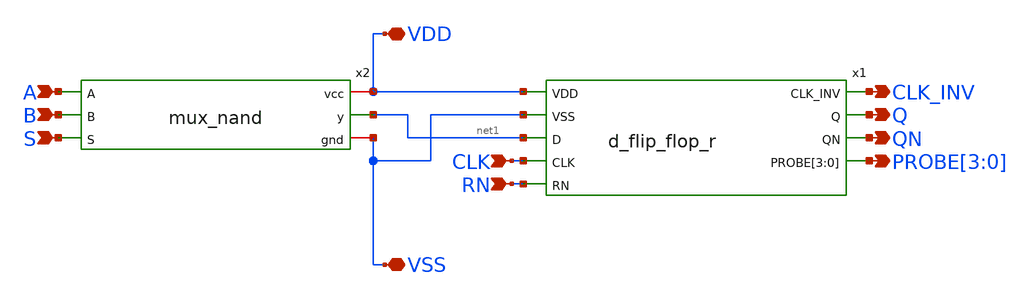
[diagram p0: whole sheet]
** sch_path: designs/schematics/sdffrq_var_nand_toplevel.sch
**.subckt sdffrq_var_nand_toplevel A B S CLK_INV VDD VSS Q QN PROBE[3],PROBE[2],PROBE[1],PROBE[0] RN
*+ CLK
*.ipin A
*.ipin B
*.ipin S
*.opin CLK_INV
*.iopin VDD
*.iopin VSS
*.opin Q
*.opin QN
*.opin PROBE[3],PROBE[2],PROBE[1],PROBE[0]
*.ipin RN
*.ipin CLK
x1 VDD CLK_INV VSS Q net1 QN CLK PROBE[3] PROBE[2] PROBE[1] PROBE[0] RN d_flip_flop_r
x2 VDD A net1 B S VSS mux_nand
**.ends

* expanding   symbol:  voidwalkers-scandff-gf180mcu/designs/schematics/d_flip_flop/d_flip_flop_r.sym
*+ # of pins=9
** sym_path: designs/schematics/d_flip_flop/d_flip_flop_r.sym
** sch_path: designs/schematics/d_flip_flop/d_flip_flop_r.sch
.subckt d_flip_flop_r VDD CLK_INV VSS Q D QN CLK PROBE[3] PROBE[2] PROBE[1] PROBE[0] RN
*.ipin D
*.ipin VDD
*.ipin VSS
*.opin Q
*.ipin CLK
*.ipin RN
*.opin CLK_INV
*.opin QN
*.opin PROBE[3],PROBE[2],PROBE[1],PROBE[0]
XM1 net1 D VDD VDD pfet_03v3 L=0.3u W=1.7u nf=1 ad='int((nf+1)/2) * W/nf * 0.18u' as='int((nf+2)/2) * W/nf * 0.18u'
+ pd='2*int((nf+1)/2) * (W/nf + 0.18u)' ps='2*int((nf+2)/2) * (W/nf + 0.18u)' nrd='0.18u / W' nrs='0.18u / W'
+ sa=0 sb=0 sd=0 m=1
XM2 PROBE[0] CLK_INV net2 VSS nfet_03v3 L=0.3u W=0.85u nf=1 ad='int((nf+1)/2) * W/nf * 0.18u' as='int((nf+2)/2) * W/nf * 0.18u'
+ pd='2*int((nf+1)/2) * (W/nf + 0.18u)' ps='2*int((nf+2)/2) * (W/nf + 0.18u)' nrd='0.18u / W' nrs='0.18u / W'
+ sa=0 sb=0 sd=0 m=1
XM3 PROBE[0] CLK net1 VDD pfet_03v3 L=0.3u W=1.7u nf=1 ad='int((nf+1)/2) * W/nf * 0.18u' as='int((nf+2)/2) * W/nf * 0.18u'
+ pd='2*int((nf+1)/2) * (W/nf + 0.18u)' ps='2*int((nf+2)/2) * (W/nf + 0.18u)' nrd='0.18u / W' nrs='0.18u / W'
+ sa=0 sb=0 sd=0 m=1
XM4 net2 D VSS VSS nfet_03v3 L=0.3u W=0.85u nf=1 ad='int((nf+1)/2) * W/nf * 0.18u' as='int((nf+2)/2) * W/nf * 0.18u'
+ pd='2*int((nf+1)/2) * (W/nf + 0.18u)' ps='2*int((nf+2)/2) * (W/nf + 0.18u)' nrd='0.18u / W' nrs='0.18u / W'
+ sa=0 sb=0 sd=0 m=1
XM5 CLK_INV CLK VDD VDD pfet_03v3 L=0.3u W=1.7u nf=1 ad='int((nf+1)/2) * W/nf * 0.18u' as='int((nf+2)/2) * W/nf * 0.18u'
+ pd='2*int((nf+1)/2) * (W/nf + 0.18u)' ps='2*int((nf+2)/2) * (W/nf + 0.18u)' nrd='0.18u / W' nrs='0.18u / W'
+ sa=0 sb=0 sd=0 m=1
XM8 CLK_INV CLK VSS VSS nfet_03v3 L=0.3u W=0.85u nf=1 ad='int((nf+1)/2) * W/nf * 0.18u' as='int((nf+2)/2) * W/nf * 0.18u'
+ pd='2*int((nf+1)/2) * (W/nf + 0.18u)' ps='2*int((nf+2)/2) * (W/nf + 0.18u)' nrd='0.18u / W' nrs='0.18u / W'
+ sa=0 sb=0 sd=0 m=1
XM13 net3 PROBE[1] VDD VDD pfet_03v3 L=0.3u W=1.7u nf=1 ad='int((nf+1)/2) * W/nf * 0.18u' as='int((nf+2)/2) * W/nf * 0.18u'
+ pd='2*int((nf+1)/2) * (W/nf + 0.18u)' ps='2*int((nf+2)/2) * (W/nf + 0.18u)' nrd='0.18u / W' nrs='0.18u / W'
+ sa=0 sb=0 sd=0 m=1
XM14 PROBE[0] CLK net4 VSS nfet_03v3 L=0.3u W=0.85u nf=1 ad='int((nf+1)/2) * W/nf * 0.18u' as='int((nf+2)/2) * W/nf * 0.18u'
+ pd='2*int((nf+1)/2) * (W/nf + 0.18u)' ps='2*int((nf+2)/2) * (W/nf + 0.18u)' nrd='0.18u / W' nrs='0.18u / W'
+ sa=0 sb=0 sd=0 m=1
XM15 PROBE[0] CLK_INV net3 VDD pfet_03v3 L=0.3u W=1.7u nf=1 ad='int((nf+1)/2) * W/nf * 0.18u' as='int((nf+2)/2) * W/nf * 0.18u'
+ pd='2*int((nf+1)/2) * (W/nf + 0.18u)' ps='2*int((nf+2)/2) * (W/nf + 0.18u)' nrd='0.18u / W' nrs='0.18u / W'
+ sa=0 sb=0 sd=0 m=1
XM16 net4 PROBE[1] VSS VSS nfet_03v3 L=0.3u W=0.85u nf=1 ad='int((nf+1)/2) * W/nf * 0.18u' as='int((nf+2)/2) * W/nf * 0.18u'
+ pd='2*int((nf+1)/2) * (W/nf + 0.18u)' ps='2*int((nf+2)/2) * (W/nf + 0.18u)' nrd='0.18u / W' nrs='0.18u / W'
+ sa=0 sb=0 sd=0 m=1
XM9 net5 PROBE[1] VDD VDD pfet_03v3 L=0.3u W=1.7u nf=1 ad='int((nf+1)/2) * W/nf * 0.18u' as='int((nf+2)/2) * W/nf * 0.18u'
+ pd='2*int((nf+1)/2) * (W/nf + 0.18u)' ps='2*int((nf+2)/2) * (W/nf + 0.18u)' nrd='0.18u / W' nrs='0.18u / W'
+ sa=0 sb=0 sd=0 m=1
XM10 PROBE[2] CLK net6 VSS nfet_03v3 L=0.3u W=0.85u nf=1 ad='int((nf+1)/2) * W/nf * 0.18u' as='int((nf+2)/2) * W/nf * 0.18u'
+ pd='2*int((nf+1)/2) * (W/nf + 0.18u)' ps='2*int((nf+2)/2) * (W/nf + 0.18u)' nrd='0.18u / W' nrs='0.18u / W'
+ sa=0 sb=0 sd=0 m=1
XM11 PROBE[2] CLK_INV net5 VDD pfet_03v3 L=0.3u W=1.7u nf=1 ad='int((nf+1)/2) * W/nf * 0.18u' as='int((nf+2)/2) * W/nf * 0.18u'
+ pd='2*int((nf+1)/2) * (W/nf + 0.18u)' ps='2*int((nf+2)/2) * (W/nf + 0.18u)' nrd='0.18u / W' nrs='0.18u / W'
+ sa=0 sb=0 sd=0 m=1
XM12 net6 PROBE[1] VSS VSS nfet_03v3 L=0.3u W=0.85u nf=1 ad='int((nf+1)/2) * W/nf * 0.18u' as='int((nf+2)/2) * W/nf * 0.18u'
+ pd='2*int((nf+1)/2) * (W/nf + 0.18u)' ps='2*int((nf+2)/2) * (W/nf + 0.18u)' nrd='0.18u / W' nrs='0.18u / W'
+ sa=0 sb=0 sd=0 m=1
XM19 net7 PROBE[3] VDD VDD pfet_03v3 L=0.3u W=1.7u nf=1 ad='int((nf+1)/2) * W/nf * 0.18u' as='int((nf+2)/2) * W/nf * 0.18u'
+ pd='2*int((nf+1)/2) * (W/nf + 0.18u)' ps='2*int((nf+2)/2) * (W/nf + 0.18u)' nrd='0.18u / W' nrs='0.18u / W'
+ sa=0 sb=0 sd=0 m=1
XM20 PROBE[2] CLK_INV net8 VSS nfet_03v3 L=0.3u W=0.85u nf=1 ad='int((nf+1)/2) * W/nf * 0.18u' as='int((nf+2)/2) * W/nf * 0.18u'
+ pd='2*int((nf+1)/2) * (W/nf + 0.18u)' ps='2*int((nf+2)/2) * (W/nf + 0.18u)' nrd='0.18u / W' nrs='0.18u / W'
+ sa=0 sb=0 sd=0 m=1
XM21 PROBE[2] CLK net7 VDD pfet_03v3 L=0.3u W=1.7u nf=1 ad='int((nf+1)/2) * W/nf * 0.18u' as='int((nf+2)/2) * W/nf * 0.18u'
+ pd='2*int((nf+1)/2) * (W/nf + 0.18u)' ps='2*int((nf+2)/2) * (W/nf + 0.18u)' nrd='0.18u / W' nrs='0.18u / W'
+ sa=0 sb=0 sd=0 m=1
XM22 net8 PROBE[3] VSS VSS nfet_03v3 L=0.3u W=0.85u nf=1 ad='int((nf+1)/2) * W/nf * 0.18u' as='int((nf+2)/2) * W/nf * 0.18u'
+ pd='2*int((nf+1)/2) * (W/nf + 0.18u)' ps='2*int((nf+2)/2) * (W/nf + 0.18u)' nrd='0.18u / W' nrs='0.18u / W'
+ sa=0 sb=0 sd=0 m=1
XM23 QN PROBE[3] VDD VDD pfet_03v3 L=0.3u W=1.7u nf=1 ad='int((nf+1)/2) * W/nf * 0.18u' as='int((nf+2)/2) * W/nf * 0.18u'
+ pd='2*int((nf+1)/2) * (W/nf + 0.18u)' ps='2*int((nf+2)/2) * (W/nf + 0.18u)' nrd='0.18u / W' nrs='0.18u / W'
+ sa=0 sb=0 sd=0 m=1
XM24 QN PROBE[3] VSS VSS nfet_03v3 L=0.3u W=0.85u nf=1 ad='int((nf+1)/2) * W/nf * 0.18u' as='int((nf+2)/2) * W/nf * 0.18u'
+ pd='2*int((nf+1)/2) * (W/nf + 0.18u)' ps='2*int((nf+2)/2) * (W/nf + 0.18u)' nrd='0.18u / W' nrs='0.18u / W'
+ sa=0 sb=0 sd=0 m=1
XM25 Q QN VDD VDD pfet_03v3 L=0.3u W=1.7u nf=1 ad='int((nf+1)/2) * W/nf * 0.18u' as='int((nf+2)/2) * W/nf * 0.18u'
+ pd='2*int((nf+1)/2) * (W/nf + 0.18u)' ps='2*int((nf+2)/2) * (W/nf + 0.18u)' nrd='0.18u / W' nrs='0.18u / W'
+ sa=0 sb=0 sd=0 m=1
XM26 Q QN VSS VSS nfet_03v3 L=0.3u W=0.85u nf=1 ad='int((nf+1)/2) * W/nf * 0.18u' as='int((nf+2)/2) * W/nf * 0.18u'
+ pd='2*int((nf+1)/2) * (W/nf + 0.18u)' ps='2*int((nf+2)/2) * (W/nf + 0.18u)' nrd='0.18u / W' nrs='0.18u / W'
+ sa=0 sb=0 sd=0 m=1
XM6 net9 PROBE[0] VDD VDD pfet_03v3 L=0.3u W=1.7u nf=1 ad='int((nf+1)/2) * W/nf * 0.18u' as='int((nf+2)/2) * W/nf * 0.18u'
+ pd='2*int((nf+1)/2) * (W/nf + 0.18u)' ps='2*int((nf+2)/2) * (W/nf + 0.18u)' nrd='0.18u / W' nrs='0.18u / W'
+ sa=0 sb=0 sd=0 m=1
XM27 PROBE[1] RN net9 VDD pfet_03v3 L=0.3u W=1.7u nf=1 ad='int((nf+1)/2) * W/nf * 0.18u' as='int((nf+2)/2) * W/nf * 0.18u'
+ pd='2*int((nf+1)/2) * (W/nf + 0.18u)' ps='2*int((nf+2)/2) * (W/nf + 0.18u)' nrd='0.18u / W' nrs='0.18u / W'
+ sa=0 sb=0 sd=0 m=1
XM28 PROBE[1] PROBE[0] VSS VSS nfet_03v3 L=0.3u W=0.85u nf=1 ad='int((nf+1)/2) * W/nf * 0.18u' as='int((nf+2)/2) * W/nf * 0.18u'
+ pd='2*int((nf+1)/2) * (W/nf + 0.18u)' ps='2*int((nf+2)/2) * (W/nf + 0.18u)' nrd='0.18u / W' nrs='0.18u / W'
+ sa=0 sb=0 sd=0 m=1
XM17 net10 PROBE[2] VDD VDD pfet_03v3 L=0.3u W=1.7u nf=1 ad='int((nf+1)/2) * W/nf * 0.18u' as='int((nf+2)/2) * W/nf * 0.18u'
+ pd='2*int((nf+1)/2) * (W/nf + 0.18u)' ps='2*int((nf+2)/2) * (W/nf + 0.18u)' nrd='0.18u / W' nrs='0.18u / W'
+ sa=0 sb=0 sd=0 m=1
XM29 PROBE[3] RN net10 VDD pfet_03v3 L=0.3u W=1.7u nf=1 ad='int((nf+1)/2) * W/nf * 0.18u' as='int((nf+2)/2) * W/nf * 0.18u'
+ pd='2*int((nf+1)/2) * (W/nf + 0.18u)' ps='2*int((nf+2)/2) * (W/nf + 0.18u)' nrd='0.18u / W' nrs='0.18u / W'
+ sa=0 sb=0 sd=0 m=1
XM30 PROBE[3] PROBE[2] VSS VSS nfet_03v3 L=0.3u W=0.85u nf=1 ad='int((nf+1)/2) * W/nf * 0.18u' as='int((nf+2)/2) * W/nf * 0.18u'
+ pd='2*int((nf+1)/2) * (W/nf + 0.18u)' ps='2*int((nf+2)/2) * (W/nf + 0.18u)' nrd='0.18u / W' nrs='0.18u / W'
+ sa=0 sb=0 sd=0 m=1
XM7 PROBE[1] RN VSS VSS nfet_03v3 L=0.3u W=0.85u nf=1 ad='int((nf+1)/2) * W/nf * 0.18u' as='int((nf+2)/2) * W/nf * 0.18u'
+ pd='2*int((nf+1)/2) * (W/nf + 0.18u)' ps='2*int((nf+2)/2) * (W/nf + 0.18u)' nrd='0.18u / W' nrs='0.18u / W'
+ sa=0 sb=0 sd=0 m=1
XM18 PROBE[3] RN VSS VSS nfet_03v3 L=0.3u W=0.85u nf=1 ad='int((nf+1)/2) * W/nf * 0.18u' as='int((nf+2)/2) * W/nf * 0.18u'
+ pd='2*int((nf+1)/2) * (W/nf + 0.18u)' ps='2*int((nf+2)/2) * (W/nf + 0.18u)' nrd='0.18u / W' nrs='0.18u / W'
+ sa=0 sb=0 sd=0 m=1
.ends


* expanding   symbol:  voidwalkers-scandff-gf180mcu/designs/schematics/mux2x1/mux_nand.sym # of
*+ pins=6
** sym_path: designs/libs/mux2x1/mux_nand.sym
** sch_path: designs/libs/mux2x1/mux_nand.sch
.subckt mux_nand vcc A y B S gnd
*.ipin S
*.ipin A
*.ipin B
*.opin y
*.iopin vcc
*.iopin gnd
x1 vcc S net1 gnd inv
x2 vcc net2 A net1 gnd nand
x3 vcc net3 B S gnd nand
x4 vcc y net2 net3 gnd nand
.ends


* expanding   symbol:  voidwalkers-scandff-gf180mcu/designs/libs/mux2x1/inv.sym # of pins=4
** sym_path: designs/schematics/mux2x1/inv.sym
** sch_path: designs/schematics/mux2x1/inv.sch
.subckt inv vcc in out gnd
*.ipin in
*.opin out
*.iopin vcc
*.iopin gnd
XM2 out in vcc vcc pfet_03v3 L=0.3u W=1.7u nf=1 ad='int((nf+1)/2) * W/nf * 0.18u' as='int((nf+2)/2) * W/nf * 0.18u'
+ pd='2*int((nf+1)/2) * (W/nf + 0.18u)' ps='2*int((nf+2)/2) * (W/nf + 0.18u)' nrd='0.18u / W' nrs='0.18u / W'
+ sa=0 sb=0 sd=0 m=1
XM1 out in gnd gnd nfet_03v3 L=0.3u W=0.85u nf=1 ad='int((nf+1)/2) * W/nf * 0.18u' as='int((nf+2)/2) * W/nf * 0.18u'
+ pd='2*int((nf+1)/2) * (W/nf + 0.18u)' ps='2*int((nf+2)/2) * (W/nf + 0.18u)' nrd='0.18u / W' nrs='0.18u / W'
+ sa=0 sb=0 sd=0 m=1
.ends


* expanding   symbol:  voidwalkers-scandff-gf180mcu/designs/libs/mux2x1/nand.sym # of pins=5
** sym_path: designs/schematics/mux2x1/nand.sym
** sch_path: designs/schematics/mux2x1/nand.sch
.subckt nand vcc OUT A B gnd
*.ipin A
*.ipin B
*.opin OUT
*.iopin vcc
*.iopin gnd
XM1 OUT B net1 gnd nfet_03v3 L=0.28u W=0.22u nf=1 ad='int((nf+1)/2) * W/nf * 0.18u' as='int((nf+2)/2) * W/nf * 0.18u'
+ pd='2*int((nf+1)/2) * (W/nf + 0.18u)' ps='2*int((nf+2)/2) * (W/nf + 0.18u)' nrd='0.18u / W' nrs='0.18u / W'
+ sa=0 sb=0 sd=0 m=1
XM2 net1 A gnd gnd nfet_03v3 L=0.28u W=0.22u nf=1 ad='int((nf+1)/2) * W/nf * 0.18u' as='int((nf+2)/2) * W/nf * 0.18u'
+ pd='2*int((nf+1)/2) * (W/nf + 0.18u)' ps='2*int((nf+2)/2) * (W/nf + 0.18u)' nrd='0.18u / W' nrs='0.18u / W'
+ sa=0 sb=0 sd=0 m=1
XM3 OUT A vcc vcc pfet_03v3 L=0.28u W=0.22u nf=1 ad='int((nf+1)/2) * W/nf * 0.18u' as='int((nf+2)/2) * W/nf * 0.18u'
+ pd='2*int((nf+1)/2) * (W/nf + 0.18u)' ps='2*int((nf+2)/2) * (W/nf + 0.18u)' nrd='0.18u / W' nrs='0.18u / W'
+ sa=0 sb=0 sd=0 m=1
XM4 OUT B vcc vcc pfet_03v3 L=0.28u W=0.22u nf=1 ad='int((nf+1)/2) * W/nf * 0.18u' as='int((nf+2)/2) * W/nf * 0.18u'
+ pd='2*int((nf+1)/2) * (W/nf + 0.18u)' ps='2*int((nf+2)/2) * (W/nf + 0.18u)' nrd='0.18u / W' nrs='0.18u / W'
+ sa=0 sb=0 sd=0 m=1
.ends

.end
